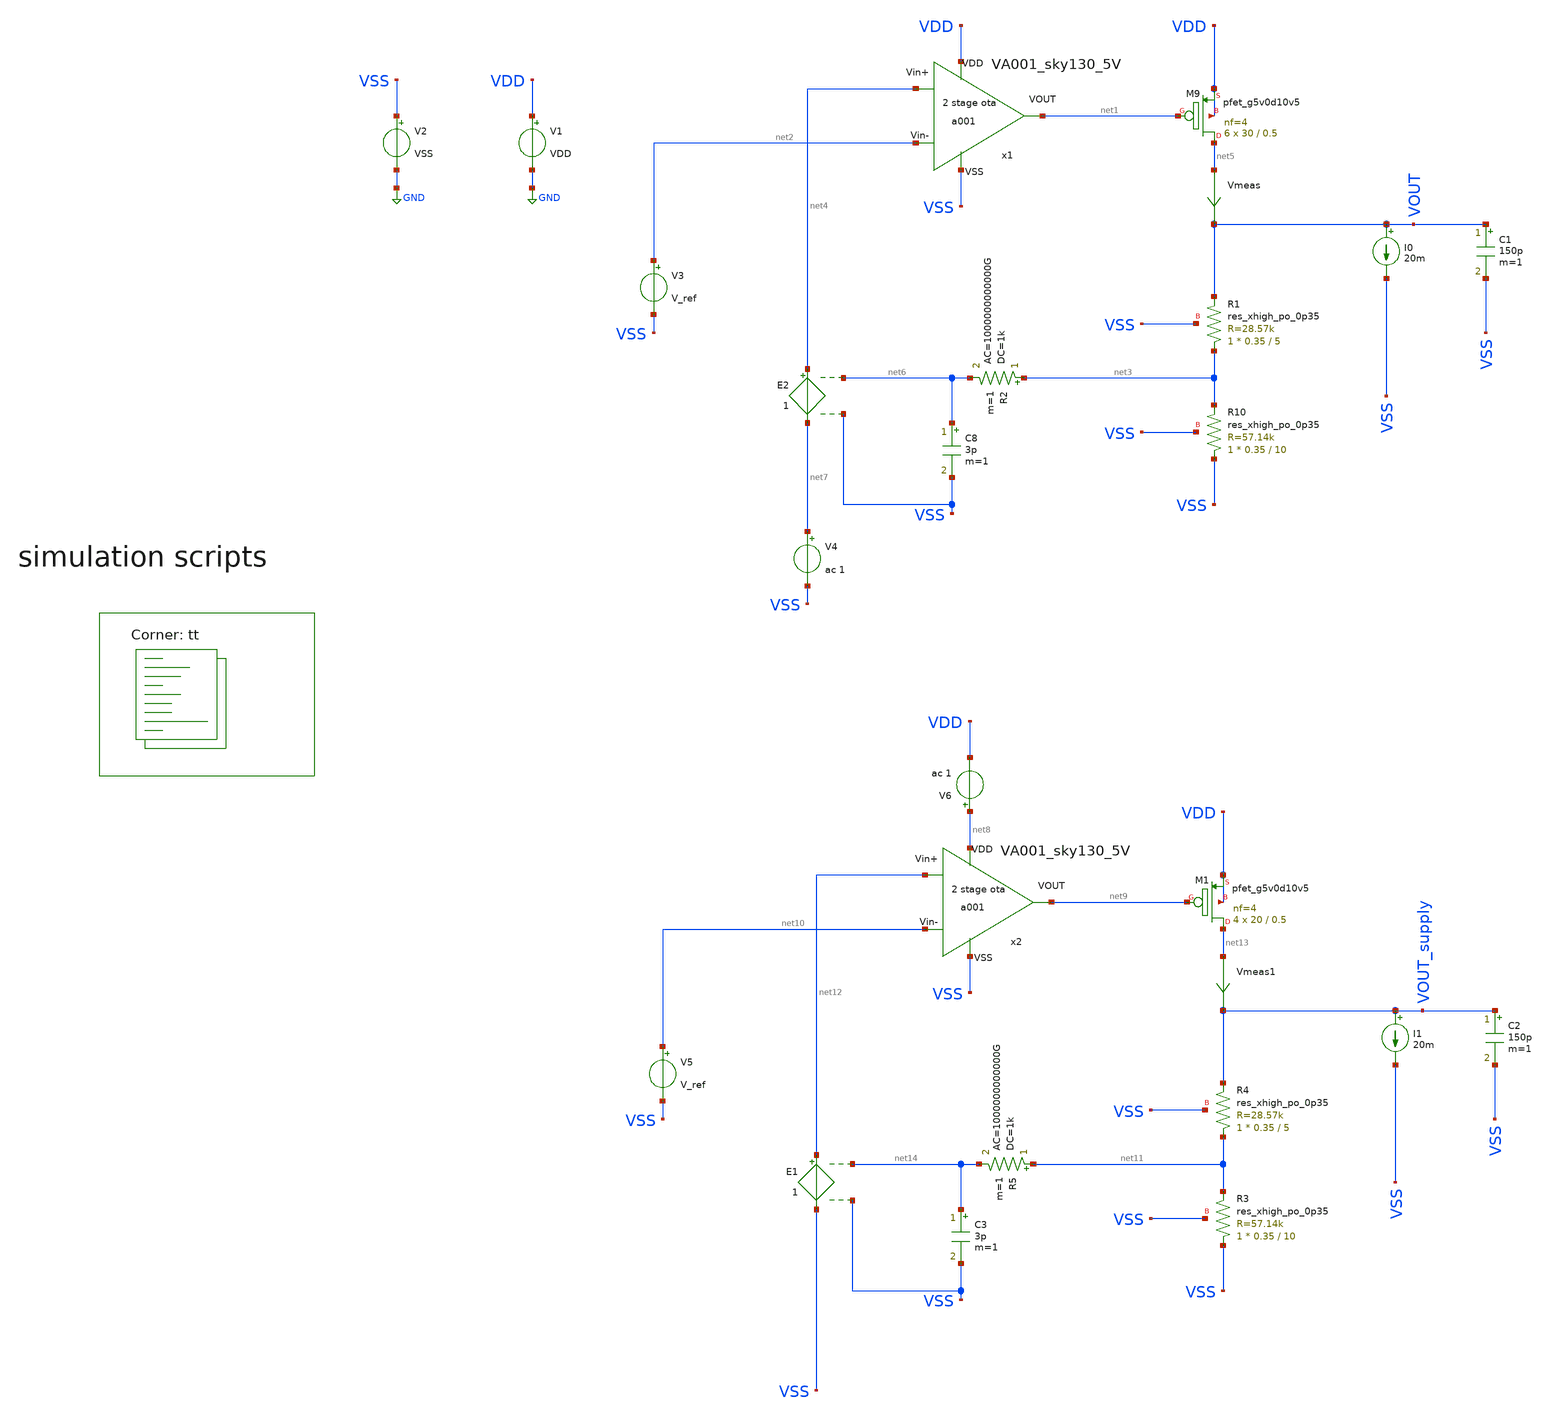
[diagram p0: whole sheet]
** sch_path: Learning/single_ended_amplifiers/Design_and_Analysis_of_Two-Stage_CMOS_Operational_Amplifier_for_Fluorescence_Signal_Processing_sky130_5V/amplifier_design/LDO_TB.sch
**.subckt LDO_TB
x1 VDD VSS net4 net2 net1 VA001_sky130_5V
V1 VDD GND VDD
V2 VSS GND VSS
XM9 net5 net1 VDD VDD sky130_fd_pr__pfet_g5v0d10v5 L=0.5 W=30 nf=4 ad='int((4 + 1)/2) * 30 / 4 * 0.29'
+ as='int((4 + 2)/2) * 30 / 4 * 0.29' pd='2*int((4 + 1)/2) * (30 / 4 + 0.29)' ps='2*int((4 + 2)/2) * (30 / 4 + 0.29)'
+ nrd='0.29 / 30 ' nrs='0.29 / 30 ' sa=0 sb=0 sd=0 mult=6 m=6
V3 net2 VSS V_ref
XR10 VSS net3 VSS sky130_fd_pr__res_xhigh_po_0p35 L=10 mult=1 m=1
XR1 net3 VOUT VSS sky130_fd_pr__res_xhigh_po_0p35 L=5 mult=1 m=1
V4 net7 VSS ac 1
C1 VOUT VSS 150p m=1
Vmeas net5 VOUT 0
.save i(vmeas)
I0 VOUT VSS 20m
R2 net3 net6 1k ac=1000000000000G m=1
C8 net6 VSS 3p m=1
E2 net4 net7 net6 VSS 1
x2 net8 VSS net12 net10 net9 VA001_sky130_5V
XM1 net13 net9 VDD VDD sky130_fd_pr__pfet_g5v0d10v5 L=0.5 W=20 nf=4 ad='int((4 + 1)/2) * 20 / 4 * 0.29'
+ as='int((4 + 2)/2) * 20 / 4 * 0.29' pd='2*int((4 + 1)/2) * (20 / 4 + 0.29)' ps='2*int((4 + 2)/2) * (20 / 4 + 0.29)'
+ nrd='0.29 / 20 ' nrs='0.29 / 20 ' sa=0 sb=0 sd=0 mult=4 m=4
V5 net10 VSS V_ref
XR3 VSS net11 VSS sky130_fd_pr__res_xhigh_po_0p35 L=10 mult=1 m=1
XR4 net11 VOUT_supply VSS sky130_fd_pr__res_xhigh_po_0p35 L=5 mult=1 m=1
C2 VOUT_supply VSS 150p m=1
Vmeas1 net13 VOUT_supply 0
.save i(vmeas1)
I1 VOUT_supply VSS 20m
R5 net11 net14 1k ac=1000000000000G m=1
C3 net14 VSS 3p m=1
E1 net12 VSS net14 VSS 1
V6 net8 VDD ac 1
**** begin user architecture code
.lib $::SKYWATER_MODELS/sky130.lib.spice tt

.Temp 27
.param VDD = 5
.param VCM = 2
.param V_ref = 1.2
.param VSS = 0
.param CL = 3p


.control

	save all
	dc V3 1 1.6 0.01
	plot v(VOUT)
	plot i(Vmeas)
	ac dec 100 1 10G
	plot db(v(VOUT)) ((180*ph(v(VOUT))/pi))
	plot (db(v(VOUT))-db(v(VOUT_supply)))
	plot db(v(VOUT_supply))

	*tran 1u 100m
	*Pplot v(VOUT)
	*plot i(Vmeas)

	dc V1 3.3 5 0.01
	plot v(VOUT)
	dc I0 0 40m 0.1m
	plot v(VOUT)


.endc


**** end user architecture code
**.ends

* expanding   symbol:  Sky130A/single ended amplifiers/VA001_sky130_5V.sym # of pins=5
** sym_path: LIB/Sky130A/single ended amplifiers/VA001_sky130_5V.sym
** sch_path: LIB/Sky130A/single ended amplifiers/VA001_sky130_5V.sch
.subckt VA001_sky130_5V VDD VSS Vin+ Vin- VOUT
*.iopin VDD
*.iopin VSS
*.iopin Vin+
*.iopin Vin-
*.iopin VOUT
XM9 VB1 VB2 net3 VSS sky130_fd_pr__nfet_g5v0d10v5 L=2 W='1 * 2 ' nf=2 ad='int((nf+1)/2) * W / nf * 0.29'
+ as='int((nf+2)/2) * W / nf * 0.29' pd='2*int((nf+1)/2) * (W / nf + 0.29)' ps='2*int((nf+2)/2) * (W / nf + 0.29)'
+ nrd='0.29 / W ' nrs='0.29 / W ' sa=0 sb=0 sd=0 mult=2 m=2
XM10 VB2 VB2 net1 VSS sky130_fd_pr__nfet_g5v0d10v5 L=2 W='1 * 2 ' nf=2 ad='int((nf+1)/2) * W / nf * 0.29'
+ as='int((nf+2)/2) * W / nf * 0.29' pd='2*int((nf+1)/2) * (W / nf + 0.29)' ps='2*int((nf+2)/2) * (W / nf + 0.29)'
+ nrd='0.29 / W ' nrs='0.29 / W ' sa=0 sb=0 sd=0 mult=2 m=2
XM3 VB2 VB1 VDD VDD sky130_fd_pr__pfet_g5v0d10v5 L=2.5 W='1 * 2 ' nf=2 ad='int((2 + 1)/2) * 1 * 0.29'
+ as='int((2 + 2)/2) * 1 * 0.29' pd='2*int((2 + 1)/2) * (1 + 0.29)' ps='2*int((2 + 2)/2) * (1 + 0.29)'
+ nrd='0.29 / 1 / 2 ' nrs='0.29 / 1 / 2 ' sa=0 sb=0 sd=0 mult=2 m=2
XM4 VB1 VB1 VDD VDD sky130_fd_pr__pfet_g5v0d10v5 L=2.5 W='1 * 2 ' nf=2 ad='int((2 + 1)/2) * 1 * 0.29'
+ as='int((2 + 2)/2) * 1 * 0.29' pd='2*int((2 + 1)/2) * (1 + 0.29)' ps='2*int((2 + 2)/2) * (1 + 0.29)'
+ nrd='0.29 / 1 / 2 ' nrs='0.29 / 1 / 2 ' sa=0 sb=0 sd=0 mult=2 m=2
XM5 net1 net1 VSS VSS sky130_fd_pr__nfet_g5v0d10v5 L=3 W='1.2 * 2 ' nf=2 ad='int((nf+1)/2) * W / nf * 0.29'
+ as='int((nf+2)/2) * W / nf * 0.29' pd='2*int((nf+1)/2) * (W / nf + 0.29)' ps='2*int((nf+2)/2) * (W / nf + 0.29)'
+ nrd='0.29 / W ' nrs='0.29 / W ' sa=0 sb=0 sd=0 mult=2 m=2
XM6 net3 net1 net2 VSS sky130_fd_pr__nfet_g5v0d10v5 L=3 W='1.2 * 2 ' nf=2 ad='int((nf+1)/2) * W / nf * 0.29'
+ as='int((nf+2)/2) * W / nf * 0.29' pd='2*int((nf+1)/2) * (W / nf + 0.29)' ps='2*int((nf+2)/2) * (W / nf + 0.29)'
+ nrd='0.29 / W ' nrs='0.29 / W ' sa=0 sb=0 sd=0 mult=8 m=8
XR2 VSS net2 VSS sky130_fd_pr__res_high_po_0p35 L=20 mult=1 m=1
XM1 net4 VB1 VDD VDD sky130_fd_pr__pfet_g5v0d10v5 L=2.5 W='1 * 2 ' nf=2 ad='int((2 + 1)/2) * 1 * 0.29'
+ as='int((2 + 2)/2) * 1 * 0.29' pd='2*int((2 + 1)/2) * (1 + 0.29)' ps='2*int((2 + 2)/2) * (1 + 0.29)'
+ nrd='0.29 / 1 / 2 ' nrs='0.29 / 1 / 2 ' sa=0 sb=0 sd=0 mult=6 m=6
XM2 net6 Vin- net4 net4 sky130_fd_pr__pfet_g5v0d10v5 L=1 W='3 * 2 ' nf=2 ad='int((2 + 1)/2) * 3 * 0.29'
+ as='int((2 + 2)/2) * 3 * 0.29' pd='2*int((2 + 1)/2) * (3 + 0.29)' ps='2*int((2 + 2)/2) * (3 + 0.29)'
+ nrd='0.29 / 3 / 2 ' nrs='0.29 / 3 / 2 ' sa=0 sb=0 sd=0 mult=4 m=4
XM11 net6 net6 VSS VSS sky130_fd_pr__nfet_g5v0d10v5 L=2 W='1.2 * 2 ' nf=2 ad='int((nf+1)/2) * W / nf * 0.29'
+ as='int((nf+2)/2) * W / nf * 0.29' pd='2*int((nf+1)/2) * (W / nf + 0.29)' ps='2*int((nf+2)/2) * (W / nf + 0.29)'
+ nrd='0.29 / W ' nrs='0.29 / W ' sa=0 sb=0 sd=0 mult=2 m=2
XM8 net5 net6 VSS VSS sky130_fd_pr__nfet_g5v0d10v5 L=2 W='1.2 * 2 ' nf=2 ad='int((nf+1)/2) * W / nf * 0.29'
+ as='int((nf+2)/2) * W / nf * 0.29' pd='2*int((nf+1)/2) * (W / nf + 0.29)' ps='2*int((nf+2)/2) * (W / nf + 0.29)'
+ nrd='0.29 / W ' nrs='0.29 / W ' sa=0 sb=0 sd=0 mult=2 m=2
XM12 VOUT net5 VSS VSS sky130_fd_pr__nfet_g5v0d10v5 L=1 W='2 * 4 ' nf=4 ad='int((nf+1)/2) * W / nf * 0.29'
+ as='int((nf+2)/2) * W / nf * 0.29' pd='2*int((nf+1)/2) * (W / nf + 0.29)' ps='2*int((nf+2)/2) * (W / nf + 0.29)'
+ nrd='0.29 / W ' nrs='0.29 / W ' sa=0 sb=0 sd=0 mult=2 m=2
XM7 net5 Vin+ net4 net4 sky130_fd_pr__pfet_g5v0d10v5 L=1 W='3 * 2 ' nf=2 ad='int((2 + 1)/2) * 3 * 0.29'
+ as='int((2 + 2)/2) * 3 * 0.29' pd='2*int((2 + 1)/2) * (3 + 0.29)' ps='2*int((2 + 2)/2) * (3 + 0.29)'
+ nrd='0.29 / 3 / 2 ' nrs='0.29 / 3 / 2 ' sa=0 sb=0 sd=0 mult=4 m=4
XM13 VOUT VB1 VDD VDD sky130_fd_pr__pfet_g5v0d10v5 L=2.5 W='1 * 2 ' nf=2 ad='int((2 + 1)/2) * 1 * 0.29'
+ as='int((2 + 2)/2) * 1 * 0.29' pd='2*int((2 + 1)/2) * (1 + 0.29)' ps='2*int((2 + 2)/2) * (1 + 0.29)'
+ nrd='0.29 / 1 / 2 ' nrs='0.29 / 1 / 2 ' sa=0 sb=0 sd=0 mult=14 m=14
XM14 net7 VB2 net5 VSS sky130_fd_pr__nfet_g5v0d10v5 L=2.1 W='1.2 * 2 ' nf=2 ad='int((nf+1)/2) * W / nf * 0.29'
+ as='int((nf+2)/2) * W / nf * 0.29' pd='2*int((nf+1)/2) * (W / nf + 0.29)' ps='2*int((nf+2)/2) * (W / nf + 0.29)'
+ nrd='0.29 / W ' nrs='0.29 / W ' sa=0 sb=0 sd=0 mult=1 m=1
XC1 net7 VOUT sky130_fd_pr__cap_mim_m3_1 W=7.5 L=7.5 MF=4 m=4
.ends

.GLOBAL GND
.end
